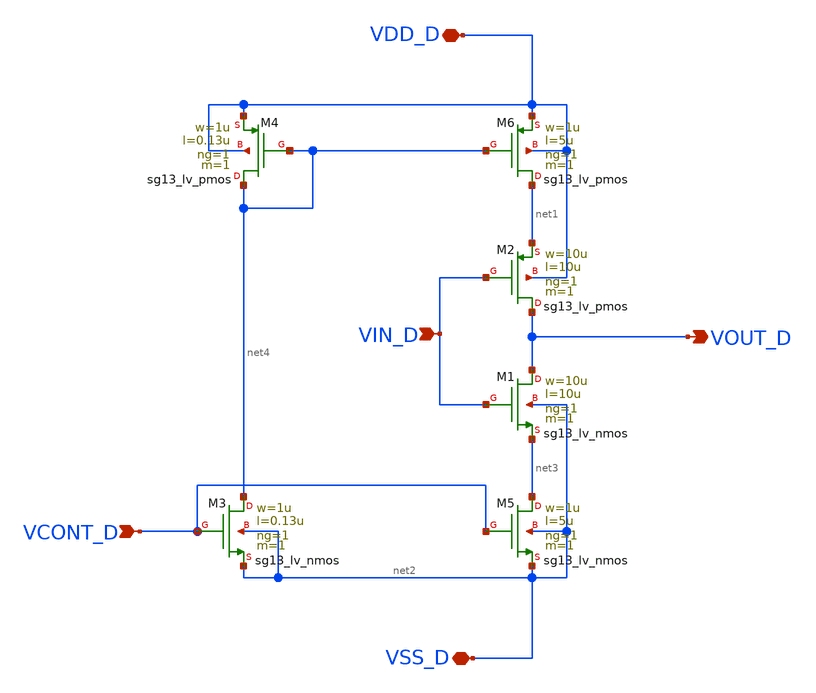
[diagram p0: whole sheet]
** sch_path: variable_delay.sch
**.subckt variable_delay VSS_D VDD_D VIN_D VOUT_D VCONT_D
*.iopin VSS_D
*.iopin VDD_D
*.ipin VIN_D
*.opin VOUT_D
*.ipin VCONT_D
XM3 net4 VCONT_D net2 net2 sg13_lv_nmos w=1u l=0.13u ng=1 m=1 mm_ok=1
XM5 net3 VCONT_D net2 net2 sg13_lv_nmos w=1u l=5u ng=1 m=1 mm_ok=1
XM4 net4 net4 VDD_D VDD_D sg13_lv_pmos w=1u l=0.13u ng=1 m=1 mm_ok=1
XM6 net1 net4 VDD_D VDD_D sg13_lv_pmos w=1u l=5u ng=1 m=1 mm_ok=1
XM2 VOUT_D VIN_D net1 VDD_D sg13_lv_pmos w=10u l=10u ng=1 m=1 mm_ok=1
XM1 VOUT_D VIN_D net3 net2 sg13_lv_nmos w=10u l=10u ng=1 m=1 mm_ok=1
**.ends
.end
